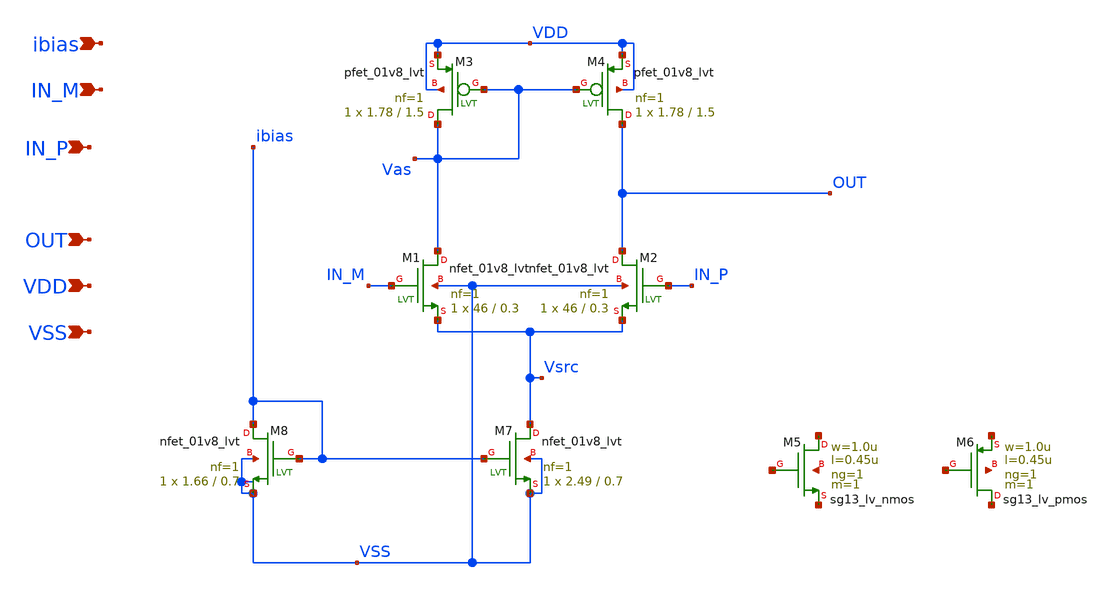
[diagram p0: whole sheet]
** sch_path: xschem/Tareas/Tarea_2/OTA1.sch
**.subckt OTA1 IN_M IN_P OUT VDD VSS ibias
*.ipin IN_M
*.ipin IN_P
*.ipin OUT
*.ipin VDD
*.ipin VSS
*.ipin ibias
XM1 Vas IN_M Vsrc VSS sky130_fd_pr__nfet_01v8_lvt L=0.3 W=46 nf=1 ad='int((nf+1)/2) * W/nf * 0.29' as='int((nf+2)/2) * W/nf * 0.29'
+ pd='2*int((nf+1)/2) * (W/nf + 0.29)' ps='2*int((nf+2)/2) * (W/nf + 0.29)' nrd='0.29 / W' nrs='0.29 / W'
+ sa=0 sb=0 sd=0 mult=1 m=1
XM2 OUT IN_P Vsrc VSS sky130_fd_pr__nfet_01v8_lvt L=0.3 W=46 nf=1 ad='int((nf+1)/2) * W/nf * 0.29' as='int((nf+2)/2) * W/nf * 0.29'
+ pd='2*int((nf+1)/2) * (W/nf + 0.29)' ps='2*int((nf+2)/2) * (W/nf + 0.29)' nrd='0.29 / W' nrs='0.29 / W'
+ sa=0 sb=0 sd=0 mult=1 m=1
XM3 Vas Vas VDD VDD sky130_fd_pr__pfet_01v8_lvt L=1.5 W=1.78 nf=1 ad='int((nf+1)/2) * W/nf * 0.29' as='int((nf+2)/2) * W/nf * 0.29'
+ pd='2*int((nf+1)/2) * (W/nf + 0.29)' ps='2*int((nf+2)/2) * (W/nf + 0.29)' nrd='0.29 / W' nrs='0.29 / W'
+ sa=0 sb=0 sd=0 mult=1 m=1
XM4 OUT Vas VDD VDD sky130_fd_pr__pfet_01v8_lvt L=1.5 W=1.78 nf=1 ad='int((nf+1)/2) * W/nf * 0.29' as='int((nf+2)/2) * W/nf * 0.29'
+ pd='2*int((nf+1)/2) * (W/nf + 0.29)' ps='2*int((nf+2)/2) * (W/nf + 0.29)' nrd='0.29 / W' nrs='0.29 / W'
+ sa=0 sb=0 sd=0 mult=1 m=1
XM7 Vsrc ibias VSS VSS sky130_fd_pr__nfet_01v8_lvt L=0.7 W=2.49 nf=1 ad='int((nf+1)/2) * W/nf * 0.29'
+ as='int((nf+2)/2) * W/nf * 0.29' pd='2*int((nf+1)/2) * (W/nf + 0.29)' ps='2*int((nf+2)/2) * (W/nf + 0.29)'
+ nrd='0.29 / W' nrs='0.29 / W' sa=0 sb=0 sd=0 mult=1 m=1
XM8 ibias ibias VSS VSS sky130_fd_pr__nfet_01v8_lvt L=0.7 W=1.66 nf=1 ad='int((nf+1)/2) * W/nf * 0.29'
+ as='int((nf+2)/2) * W/nf * 0.29' pd='2*int((nf+1)/2) * (W/nf + 0.29)' ps='2*int((nf+2)/2) * (W/nf + 0.29)'
+ nrd='0.29 / W' nrs='0.29 / W' sa=0 sb=0 sd=0 mult=1 m=1
XM5 net1 net2 net3 net4 sg13_lv_nmos w=1.0u l=0.45u ng=1 m=1 mm_ok=1
XM6 net5 net6 net7 net8 sg13_lv_pmos w=1.0u l=0.45u ng=1 m=1 mm_ok=1
**.ends
.end
